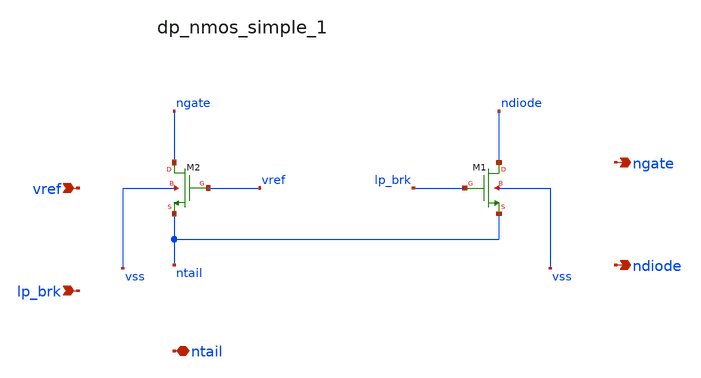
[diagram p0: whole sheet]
** sch_path: analog-db/raw/ldo_003_analoggym_simple/hier/blocks/dp_nmos_simple_1.sch
**.subckt dp_nmos_simple_1 vref lp_brk ntail ngate ndiode
*.ipin vref
*.ipin lp_brk
*.iopin ntail
*.opin ngate
*.opin ndiode
XM1 ndiode lp_brk ntail vss sg13_hv_nmos w=x_dut_xm1_w l=x_dut_xm1_l ng=1 m=1
XM2 ngate vref ntail vss sg13_hv_nmos w=x_dut_xm2_w l=x_dut_xm2_l ng=1 m=1
**.ends
.end
